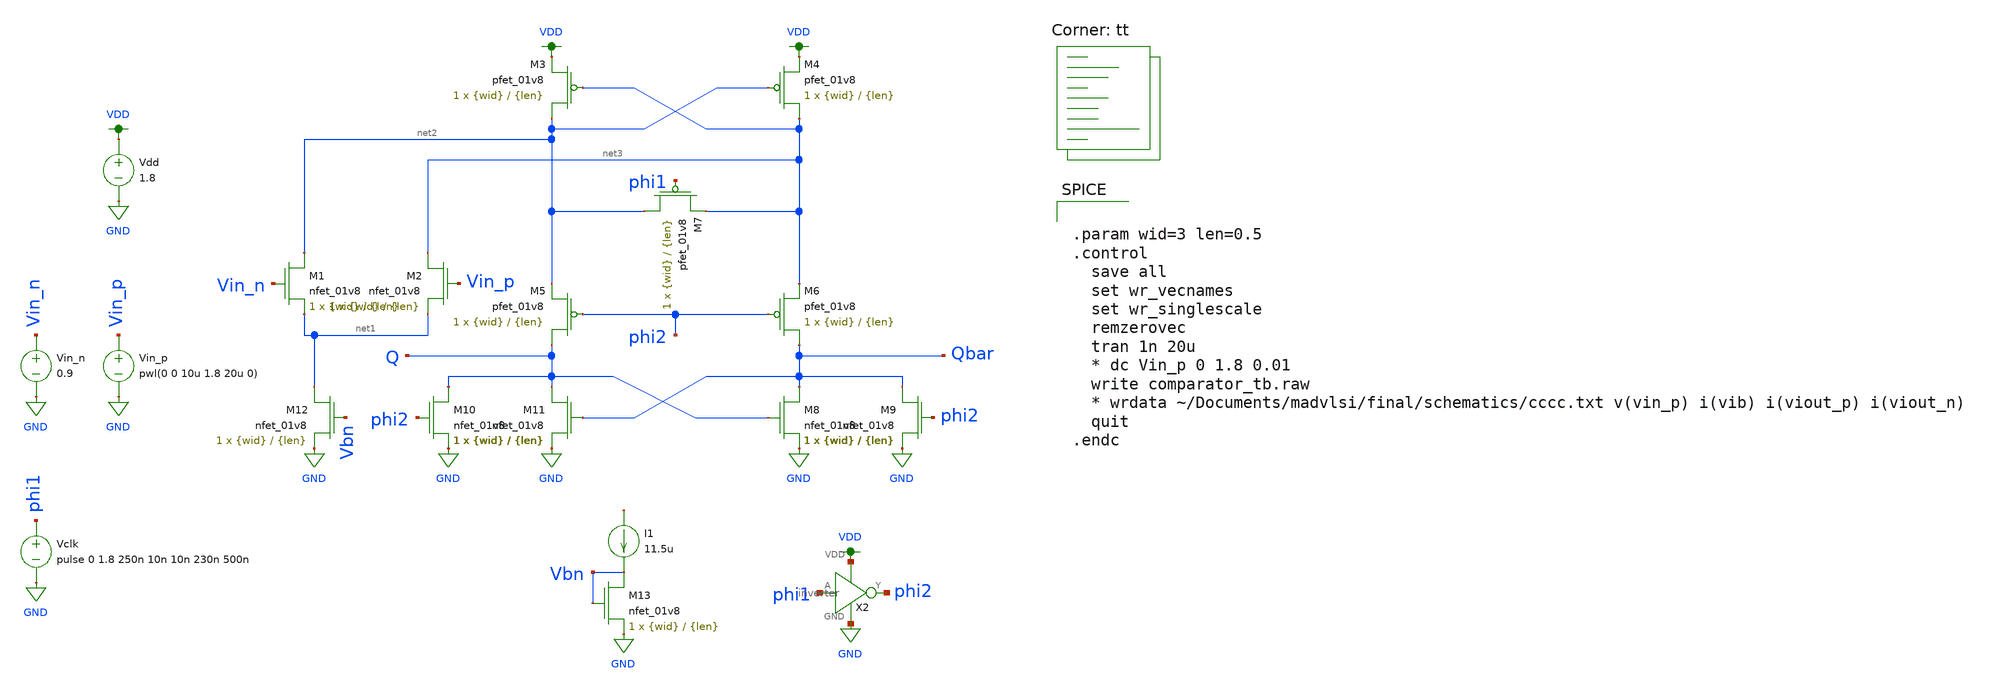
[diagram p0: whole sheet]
** sch_path: final/schematics/comparator_tb.sch
**.subckt comparator_tb
XM1 net2 Vin_n net1 GND sky130_fd_pr__nfet_01v8 L={len} W={wid} nf=1 ad='int((nf+1)/2) * W/nf * 0.29'
+ as='int((nf+2)/2) * W/nf * 0.29' pd='2*int((nf+1)/2) * (W/nf + 0.29)' ps='2*int((nf+2)/2) * (W/nf + 0.29)'
+ nrd='0.29 / W' nrs='0.29 / W' sa=0 sb=0 sd=0 mult=1 m=1
XM6 Qbar phi2 net3 VDD sky130_fd_pr__pfet_01v8 L={len} W={wid} nf=1 ad='int((nf+1)/2) * W/nf * 0.29'
+ as='int((nf+2)/2) * W/nf * 0.29' pd='2*int((nf+1)/2) * (W/nf + 0.29)' ps='2*int((nf+2)/2) * (W/nf + 0.29)'
+ nrd='0.29 / W' nrs='0.29 / W' sa=0 sb=0 sd=0 mult=1 m=1
XM7 net2 phi1 net3 VDD sky130_fd_pr__pfet_01v8 L={len} W={wid} nf=1 ad='int((nf+1)/2) * W/nf * 0.29'
+ as='int((nf+2)/2) * W/nf * 0.29' pd='2*int((nf+1)/2) * (W/nf + 0.29)' ps='2*int((nf+2)/2) * (W/nf + 0.29)'
+ nrd='0.29 / W' nrs='0.29 / W' sa=0 sb=0 sd=0 mult=1 m=1
XM2 net3 Vin_p net1 GND sky130_fd_pr__nfet_01v8 L={len} W={wid} nf=1 ad='int((nf+1)/2) * W/nf * 0.29'
+ as='int((nf+2)/2) * W/nf * 0.29' pd='2*int((nf+1)/2) * (W/nf + 0.29)' ps='2*int((nf+2)/2) * (W/nf + 0.29)'
+ nrd='0.29 / W' nrs='0.29 / W' sa=0 sb=0 sd=0 mult=1 m=1
XM12 net1 Vbn GND GND sky130_fd_pr__nfet_01v8 L={len} W={wid} nf=1 ad='int((nf+1)/2) * W/nf * 0.29' as='int((nf+2)/2) * W/nf * 0.29'
+ pd='2*int((nf+1)/2) * (W/nf + 0.29)' ps='2*int((nf+2)/2) * (W/nf + 0.29)' nrd='0.29 / W' nrs='0.29 / W'
+ sa=0 sb=0 sd=0 mult=1 m=1
XM10 Q phi2 GND GND sky130_fd_pr__nfet_01v8 L={len} W={wid} nf=1 ad='int((nf+1)/2) * W/nf * 0.29' as='int((nf+2)/2) * W/nf * 0.29'
+ pd='2*int((nf+1)/2) * (W/nf + 0.29)' ps='2*int((nf+2)/2) * (W/nf + 0.29)' nrd='0.29 / W' nrs='0.29 / W'
+ sa=0 sb=0 sd=0 mult=1 m=1
XM11 Q Qbar GND GND sky130_fd_pr__nfet_01v8 L={len} W={wid} nf=1 ad='int((nf+1)/2) * W/nf * 0.29' as='int((nf+2)/2) * W/nf * 0.29'
+ pd='2*int((nf+1)/2) * (W/nf + 0.29)' ps='2*int((nf+2)/2) * (W/nf + 0.29)' nrd='0.29 / W' nrs='0.29 / W'
+ sa=0 sb=0 sd=0 mult=1 m=1
XM8 Qbar Q GND GND sky130_fd_pr__nfet_01v8 L={len} W={wid} nf=1 ad='int((nf+1)/2) * W/nf * 0.29' as='int((nf+2)/2) * W/nf * 0.29'
+ pd='2*int((nf+1)/2) * (W/nf + 0.29)' ps='2*int((nf+2)/2) * (W/nf + 0.29)' nrd='0.29 / W' nrs='0.29 / W'
+ sa=0 sb=0 sd=0 mult=1 m=1
XM9 Qbar phi2 GND GND sky130_fd_pr__nfet_01v8 L={len} W={wid} nf=1 ad='int((nf+1)/2) * W/nf * 0.29' as='int((nf+2)/2) * W/nf * 0.29'
+ pd='2*int((nf+1)/2) * (W/nf + 0.29)' ps='2*int((nf+2)/2) * (W/nf + 0.29)' nrd='0.29 / W' nrs='0.29 / W'
+ sa=0 sb=0 sd=0 mult=1 m=1
XM5 Q phi2 net2 VDD sky130_fd_pr__pfet_01v8 L={len} W={wid} nf=1 ad='int((nf+1)/2) * W/nf * 0.29' as='int((nf+2)/2) * W/nf * 0.29'
+ pd='2*int((nf+1)/2) * (W/nf + 0.29)' ps='2*int((nf+2)/2) * (W/nf + 0.29)' nrd='0.29 / W' nrs='0.29 / W'
+ sa=0 sb=0 sd=0 mult=1 m=1
XM3 net2 net3 VDD VDD sky130_fd_pr__pfet_01v8 L={len} W={wid} nf=1 ad='int((nf+1)/2) * W/nf * 0.29' as='int((nf+2)/2) * W/nf * 0.29'
+ pd='2*int((nf+1)/2) * (W/nf + 0.29)' ps='2*int((nf+2)/2) * (W/nf + 0.29)' nrd='0.29 / W' nrs='0.29 / W'
+ sa=0 sb=0 sd=0 mult=1 m=1
XM4 net3 net2 VDD VDD sky130_fd_pr__pfet_01v8 L={len} W={wid} nf=1 ad='int((nf+1)/2) * W/nf * 0.29' as='int((nf+2)/2) * W/nf * 0.29'
+ pd='2*int((nf+1)/2) * (W/nf + 0.29)' ps='2*int((nf+2)/2) * (W/nf + 0.29)' nrd='0.29 / W' nrs='0.29 / W'
+ sa=0 sb=0 sd=0 mult=1 m=1
Vdd VDD GND 1.8
Vclk phi1 GND pulse 0 1.8 250n 10n 10n 230n 500n
Vin_n Vin_n GND 0.9
Vin_p Vin_p GND pwl(0 0 10u 1.8 20u 0)
XM13 Vbn Vbn GND GND sky130_fd_pr__nfet_01v8 L={len} W={wid} nf=1 ad='int((nf+1)/2) * W/nf * 0.29' as='int((nf+2)/2) * W/nf * 0.29'
+ pd='2*int((nf+1)/2) * (W/nf + 0.29)' ps='2*int((nf+2)/2) * (W/nf + 0.29)' nrd='0.29 / W' nrs='0.29 / W'
+ sa=0 sb=0 sd=0 mult=1 m=1
I1 net4 Vbn 11.5u
X2 VDD phi1 phi2 GND inverter
**** begin user architecture code


.param wid=3 len=0.5
.control
  save all
  set wr_vecnames
  set wr_singlescale
  remzerovec
  tran 1n 20u
  * dc Vin_p 0 1.8 0.01
  write comparator_tb.raw
  * wrdata ~/Documents/madvlsi/final/schematics/cccc.txt v(vin_p) i(vib) i(viout_p) i(viout_n)
  quit
.endc


.lib $::SKYWATER_MODELS/sky130.lib.spice tt
**** end user architecture code
**.ends

* expanding   symbol:  inverter.sym # of pins=4
** sym_path: final/schematics/inverter.sym
** sch_path: final/schematics/inverter.sch
.subckt inverter VDD A Y GND
*.ipin A
*.iopin VDD
*.iopin GND
*.opin Y
XM1 Y A GND GND sky130_fd_pr__nfet_01v8 L={len} W={wid} nf=1 ad='int((nf+1)/2) * W/nf * 0.29' as='int((nf+2)/2) * W/nf * 0.29'
+ pd='2*int((nf+1)/2) * (W/nf + 0.29)' ps='2*int((nf+2)/2) * (W/nf + 0.29)' nrd='0.29 / W' nrs='0.29 / W'
+ sa=0 sb=0 sd=0 mult=1 m=1
XM2 Y A VDD VDD sky130_fd_pr__pfet_01v8 L={len} W={wid} nf=1 ad='int((nf+1)/2) * W/nf * 0.29' as='int((nf+2)/2) * W/nf * 0.29'
+ pd='2*int((nf+1)/2) * (W/nf + 0.29)' ps='2*int((nf+2)/2) * (W/nf + 0.29)' nrd='0.29 / W' nrs='0.29 / W'
+ sa=0 sb=0 sd=0 mult=1 m=1
**** begin user architecture code


.param wid=3 len=0.5


**** end user architecture code
.ends

.GLOBAL VDD
.GLOBAL GND
.end
